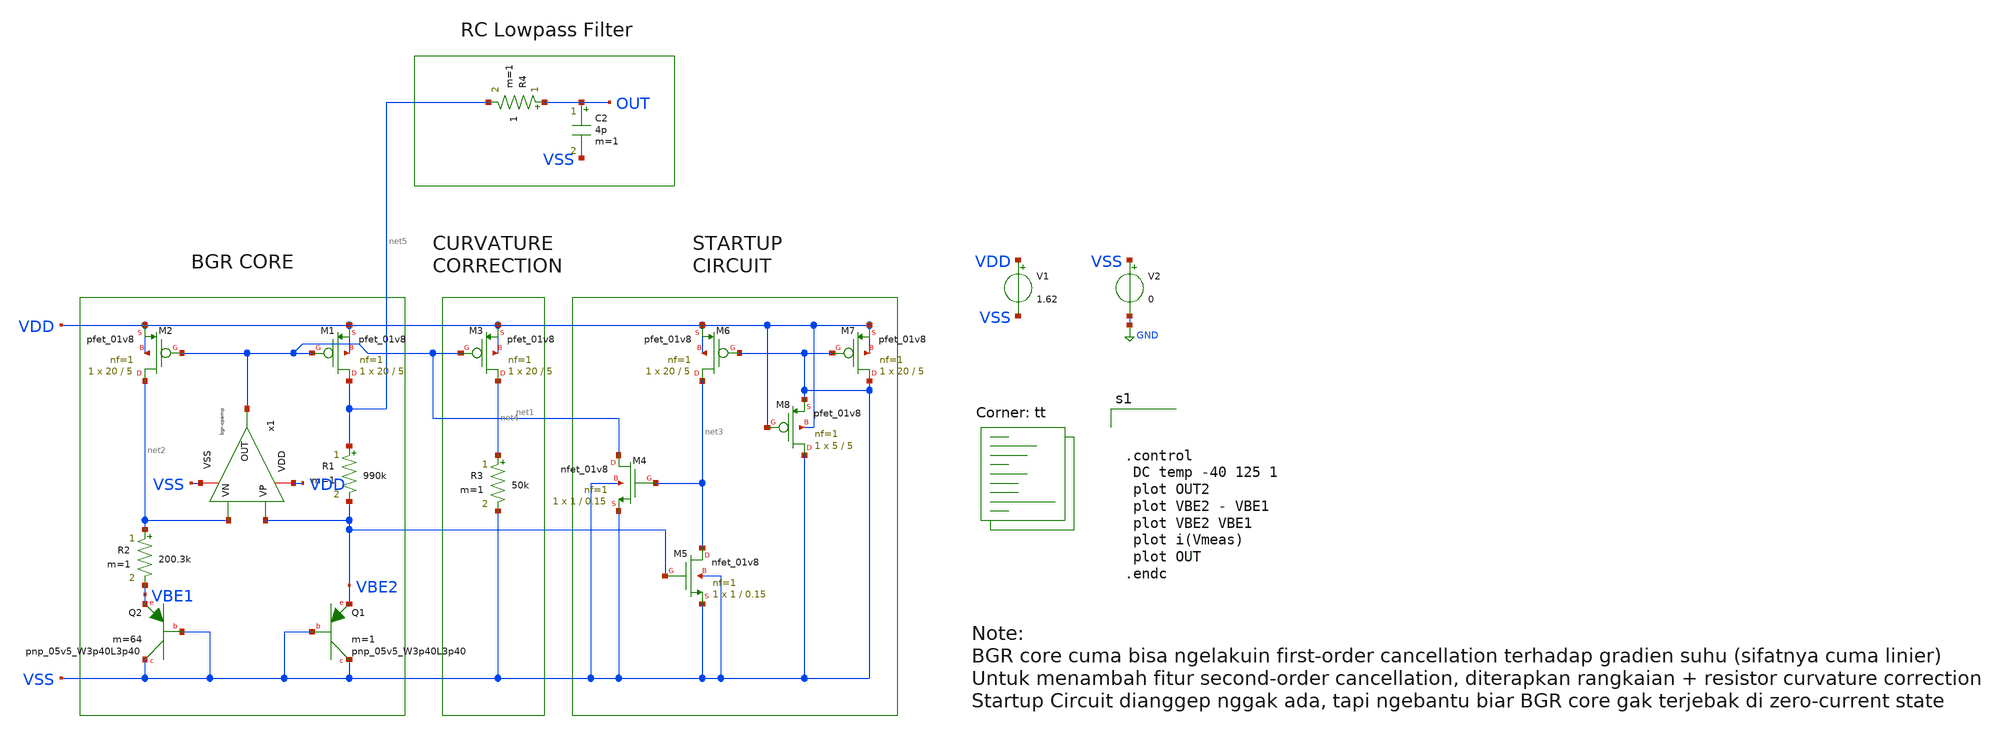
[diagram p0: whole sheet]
** sch_path: bandgap/bgr2.sch
**.subckt bgr2
x1 VDD net1 VBE2 net2 VSS bgr-opamp
XM1 net5 net1 VDD VDD sky130_fd_pr__pfet_01v8 L=5 W=20 nf=1 ad='int((nf+1)/2) * W/nf * 0.29' as='int((nf+2)/2) * W/nf * 0.29'
+ pd='2*int((nf+1)/2) * (W/nf + 0.29)' ps='2*int((nf+2)/2) * (W/nf + 0.29)' nrd='0.29 / W' nrs='0.29 / W'
+ sa=0 sb=0 sd=0 mult=1 m=1
XM2 net2 net1 VDD VDD sky130_fd_pr__pfet_01v8 L=5 W=20 nf=1 ad='int((nf+1)/2) * W/nf * 0.29' as='int((nf+2)/2) * W/nf * 0.29'
+ pd='2*int((nf+1)/2) * (W/nf + 0.29)' ps='2*int((nf+2)/2) * (W/nf + 0.29)' nrd='0.29 / W' nrs='0.29 / W'
+ sa=0 sb=0 sd=0 mult=1 m=1
R1 net5 VBE2 990k m=1
R2 net2 VBE1 200.3k m=1
XQ1 VSS VSS VBE2 sky130_fd_pr__pnp_05v5_W3p40L3p40 m=1
XQ2 VSS VSS VBE1 sky130_fd_pr__pnp_05v5_W3p40L3p40 m=64
V1 VDD VSS 1.62
V2 VSS GND 0
XM3 net4 net1 VDD VDD sky130_fd_pr__pfet_01v8 L=5 W=20 nf=1 ad='int((nf+1)/2) * W/nf * 0.29' as='int((nf+2)/2) * W/nf * 0.29'
+ pd='2*int((nf+1)/2) * (W/nf + 0.29)' ps='2*int((nf+2)/2) * (W/nf + 0.29)' nrd='0.29 / W' nrs='0.29 / W'
+ sa=0 sb=0 sd=0 mult=1 m=1
R3 net4 VSS 50k m=1
XM4 net1 net3 VSS VSS sky130_fd_pr__nfet_01v8 L=0.15 W=1 nf=1 ad='int((nf+1)/2) * W/nf * 0.29' as='int((nf+2)/2) * W/nf * 0.29'
+ pd='2*int((nf+1)/2) * (W/nf + 0.29)' ps='2*int((nf+2)/2) * (W/nf + 0.29)' nrd='0.29 / W' nrs='0.29 / W'
+ sa=0 sb=0 sd=0 mult=1 m=1
XM5 net3 VBE2 VSS VSS sky130_fd_pr__nfet_01v8 L=0.15 W=1 nf=1 ad='int((nf+1)/2) * W/nf * 0.29' as='int((nf+2)/2) * W/nf * 0.29'
+ pd='2*int((nf+1)/2) * (W/nf + 0.29)' ps='2*int((nf+2)/2) * (W/nf + 0.29)' nrd='0.29 / W' nrs='0.29 / W'
+ sa=0 sb=0 sd=0 mult=1 m=1
XM6 net3 VSS VDD VDD sky130_fd_pr__pfet_01v8 L=5 W=20 nf=1 ad='int((nf+1)/2) * W/nf * 0.29' as='int((nf+2)/2) * W/nf * 0.29'
+ pd='2*int((nf+1)/2) * (W/nf + 0.29)' ps='2*int((nf+2)/2) * (W/nf + 0.29)' nrd='0.29 / W' nrs='0.29 / W'
+ sa=0 sb=0 sd=0 mult=1 m=1
XM7 VSS VSS VDD VDD sky130_fd_pr__pfet_01v8 L=5 W=20 nf=1 ad='int((nf+1)/2) * W/nf * 0.29' as='int((nf+2)/2) * W/nf * 0.29'
+ pd='2*int((nf+1)/2) * (W/nf + 0.29)' ps='2*int((nf+2)/2) * (W/nf + 0.29)' nrd='0.29 / W' nrs='0.29 / W'
+ sa=0 sb=0 sd=0 mult=1 m=1
XM8 VSS VDD VSS VDD sky130_fd_pr__pfet_01v8 L=5 W=5 nf=1 ad='int((nf+1)/2) * W/nf * 0.29' as='int((nf+2)/2) * W/nf * 0.29'
+ pd='2*int((nf+1)/2) * (W/nf + 0.29)' ps='2*int((nf+2)/2) * (W/nf + 0.29)' nrd='0.29 / W' nrs='0.29 / W'
+ sa=0 sb=0 sd=0 mult=1 m=1
C2 OUT VSS 4p m=1
R4 OUT net5 1 m=1
**** begin user architecture code
.lib $::SKYWATER_MODELS/sky130.lib.spice tt



.control
 DC temp -40 125 1
 plot OUT2
 plot VBE2 - VBE1
 plot VBE2 VBE1
 plot i(Vmeas)
 plot OUT
.endc


**** end user architecture code
**.ends

* expanding   symbol:  afe-icdec-teknofest-2026/bandgap/bgr-opamp/bgr-opamp.sym # of pins=5
** sym_path: bandgap/bgr-opamp/bgr-opamp.sym
** sch_path: bandgap/bgr-opamp/bgr-opamp.sch
.subckt bgr-opamp VDD OUT VP VN VSS
*.iopin VSS
*.iopin VDD
*.ipin VP
*.ipin VN
*.opin OUT
XM1 net1 VP net3 VSS sky130_fd_pr__nfet_01v8 L=0.3 W=2.5 nf=2 ad='int((nf+1)/2) * W/nf * 0.29' as='int((nf+2)/2) * W/nf * 0.29'
+ pd='2*int((nf+1)/2) * (W/nf + 0.29)' ps='2*int((nf+2)/2) * (W/nf + 0.29)' nrd='0.29 / W' nrs='0.29 / W'
+ sa=0 sb=0 sd=0 mult=1 m=1
XM2 net2 VN net3 VSS sky130_fd_pr__nfet_01v8 L=0.3 W=2.5 nf=2 ad='int((nf+1)/2) * W/nf * 0.29' as='int((nf+2)/2) * W/nf * 0.29'
+ pd='2*int((nf+1)/2) * (W/nf + 0.29)' ps='2*int((nf+2)/2) * (W/nf + 0.29)' nrd='0.29 / W' nrs='0.29 / W'
+ sa=0 sb=0 sd=0 mult=1 m=1
XM4 net2 net1 VDD VDD sky130_fd_pr__pfet_01v8 L=1.25 W=10.8 nf=4 ad='int((nf+1)/2) * W/nf * 0.29' as='int((nf+2)/2) * W/nf * 0.29'
+ pd='2*int((nf+1)/2) * (W/nf + 0.29)' ps='2*int((nf+2)/2) * (W/nf + 0.29)' nrd='0.29 / W' nrs='0.29 / W'
+ sa=0 sb=0 sd=0 mult=1 m=1
XM3 net1 net1 VDD VDD sky130_fd_pr__pfet_01v8 L=1.25 W=10.8 nf=4 ad='int((nf+1)/2) * W/nf * 0.29' as='int((nf+2)/2) * W/nf * 0.29'
+ pd='2*int((nf+1)/2) * (W/nf + 0.29)' ps='2*int((nf+2)/2) * (W/nf + 0.29)' nrd='0.29 / W' nrs='0.29 / W'
+ sa=0 sb=0 sd=0 mult=1 m=1
XM5 net3 net4 VSS VSS sky130_fd_pr__nfet_01v8 L=1.25 W=3.4 nf=1 ad='int((nf+1)/2) * W/nf * 0.29' as='int((nf+2)/2) * W/nf * 0.29'
+ pd='2*int((nf+1)/2) * (W/nf + 0.29)' ps='2*int((nf+2)/2) * (W/nf + 0.29)' nrd='0.29 / W' nrs='0.29 / W'
+ sa=0 sb=0 sd=0 mult=1 m=1
XM9 net4 net6 net5 net5 sky130_fd_pr__nfet_01v8 L=1.25 W=3.4 nf=1 ad='int((nf+1)/2) * W/nf * 0.29' as='int((nf+2)/2) * W/nf * 0.29'
+ pd='2*int((nf+1)/2) * (W/nf + 0.29)' ps='2*int((nf+2)/2) * (W/nf + 0.29)' nrd='0.29 / W' nrs='0.29 / W'
+ sa=0 sb=0 sd=0 mult=1 m=1
XM8 net4 net4 VDD VDD sky130_fd_pr__pfet_01v8 L=1.25 W=10.8 nf=4 ad='int((nf+1)/2) * W/nf * 0.29' as='int((nf+2)/2) * W/nf * 0.29'
+ pd='2*int((nf+1)/2) * (W/nf + 0.29)' ps='2*int((nf+2)/2) * (W/nf + 0.29)' nrd='0.29 / W' nrs='0.29 / W'
+ sa=0 sb=0 sd=0 mult=1 m=1
XM11 net6 net4 VDD VDD sky130_fd_pr__pfet_01v8 L=1.25 W=10.8 nf=4 ad='int((nf+1)/2) * W/nf * 0.29' as='int((nf+2)/2) * W/nf * 0.29'
+ pd='2*int((nf+1)/2) * (W/nf + 0.29)' ps='2*int((nf+2)/2) * (W/nf + 0.29)' nrd='0.29 / W' nrs='0.29 / W'
+ sa=0 sb=0 sd=0 mult=1 m=1
XM10 net6 net6 VSS VSS sky130_fd_pr__nfet_01v8 L=1.25 W=3.4 nf=1 ad='int((nf+1)/2) * W/nf * 0.29' as='int((nf+2)/2) * W/nf * 0.29'
+ pd='2*int((nf+1)/2) * (W/nf + 0.29)' ps='2*int((nf+2)/2) * (W/nf + 0.29)' nrd='0.29 / W' nrs='0.29 / W'
+ sa=0 sb=0 sd=0 mult=1 m=1
XM6 OUT net2 VDD VDD sky130_fd_pr__pfet_01v8 L=1.25 W=110 nf=32 ad='int((nf+1)/2) * W/nf * 0.29' as='int((nf+2)/2) * W/nf * 0.29'
+ pd='2*int((nf+1)/2) * (W/nf + 0.29)' ps='2*int((nf+2)/2) * (W/nf + 0.29)' nrd='0.29 / W' nrs='0.29 / W'
+ sa=0 sb=0 sd=0 mult=1 m=1
XM7 OUT net4 VSS VSS sky130_fd_pr__nfet_01v8 L=1.25 W=12 nf=4 ad='int((nf+1)/2) * W/nf * 0.29' as='int((nf+2)/2) * W/nf * 0.29'
+ pd='2*int((nf+1)/2) * (W/nf + 0.29)' ps='2*int((nf+2)/2) * (W/nf + 0.29)' nrd='0.29 / W' nrs='0.29 / W'
+ sa=0 sb=0 sd=0 mult=1 m=1
XC2 OUT net2 sky130_fd_pr__cap_mim_m3_1 W=20 L=20 MF=4 m=4
XM12 net4 net4 net6 net6 sky130_fd_pr__nfet_01v8 L=0.15 W=0.85 nf=1 ad='int((nf+1)/2) * W/nf * 0.29'
+ as='int((nf+2)/2) * W/nf * 0.29' pd='2*int((nf+1)/2) * (W/nf + 0.29)' ps='2*int((nf+2)/2) * (W/nf + 0.29)'
+ nrd='0.29 / W' nrs='0.29 / W' sa=0 sb=0 sd=0 mult=1 m=1
XR2 net7 net5 VSS sky130_fd_pr__res_high_po_1p41 L=3.235 mult=1 m=1
XR3 net9 net7 VSS sky130_fd_pr__res_high_po_1p41 L=3.235 mult=1 m=1
XR4 net8 net9 VSS sky130_fd_pr__res_high_po_1p41 L=3.235 mult=1 m=1
XR5 net10 net8 VSS sky130_fd_pr__res_high_po_1p41 L=3.235 mult=1 m=1
XR6 VSS net10 VSS sky130_fd_pr__res_high_po_1p41 L=3.235 mult=1 m=1
.ends

.GLOBAL GND
.end
